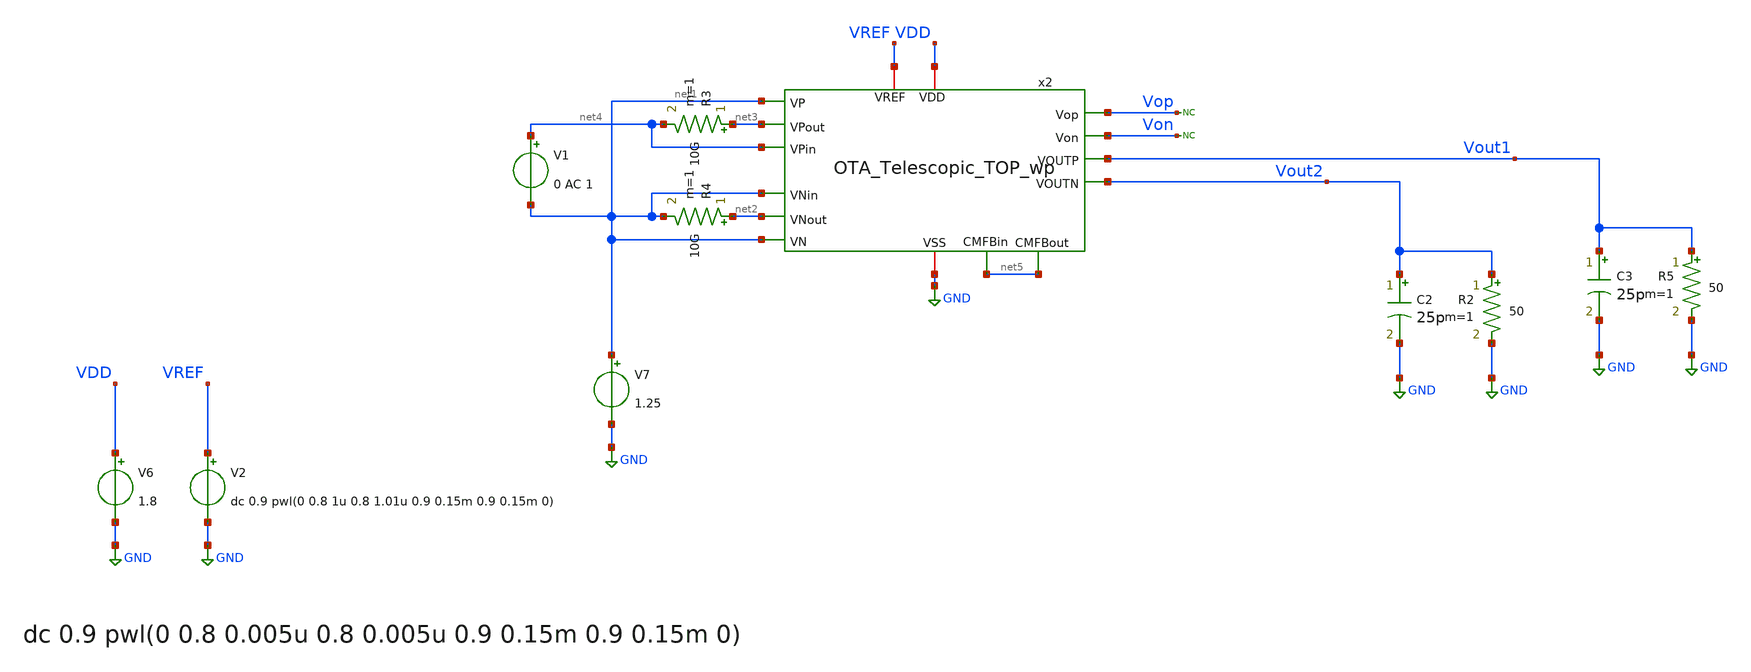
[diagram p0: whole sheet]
** sch_path: OTA_Telescopic_backup/OTA_Telescopic_NO_FLATTEN/Testbenchs/OTA_Telescopic_TOP_TB_OL.sch
**.subckt OTA_Telescopic_TOP_TB_OL
V7 net1 GND 1.25
C2 Vout2 GND 25p m=1
V6 VDD GND 1.8
R3 net3 net4 10G m=1
R4 net2 net1 10G m=1
V1 net4 net1 0 AC 1
V2 VREF GND dc 0.9 pwl(0 0.8 1u 0.8 1.01u 0.9 0.15m 0.9 0.15m 0)
x2 VDD GND net3 net4 Vout1 net1 net1 Vout2 net1 net2 net5 VREF net5 Vop Von OTA_Telescopic_TOP_wp
R2 Vout2 GND 50 m=1
C3 Vout1 GND 25p m=1
R5 Vout1 GND 50 m=1
* noconn Vop
* noconn Von
**** begin user architecture code

** opencircuitdesign pdks install
.lib cornerMOSlv.lib mos_tt
.lib cornerRES.lib res_typ
.lib cornerCAP.lib cap_typ
.temp 65



.control
save all
 set color0 = white

* AC simulation
ac dec 1k 1 1T
let Av = db((v(von)-v(vop)))
meas ac Ao FIND Av WHEN frequency=10
let ABW = Ao-3
meas ac BW WHEN Av=ABW
meas ac UGBW WHEN Av=0
let phase_vec = 180/pi*cph(v(von)-v(vop))

* Phase margin (PM)
meas ac phase FIND phase_vec WHEN frequency=UGBW
let PM = phase+180
print PM

* Gain margin (GM)
meas ac freq180 FIND frequency WHEN phase_vec=-180
meas ac gain FIND Av WHEN frequency=freq180
let GM = 0-gain

*BW in 7 dB
meas ac UGBW7dB WHEN Av=7
meas ac UGBW4dB WHEN Av=4

print GM
plot Av
plot phase_vec

write AC_OL.raw

wrdata AvOL_ Av
wrdata PhaseOL_ phase_vec


*DC simulation

op
let vout_dc = v(Vout1)
print vout_dc
write OTA_Telescopic_TOP_TB_OL.raw


reset
noise v(Vout1) V6 dec 100 1 0.5e9 1
setplot noise1
*plot onoise_spectrum
setplot noise2
print onoise_total

.endc


**** end user architecture code
**.ends
.GLOBAL GND
.end
